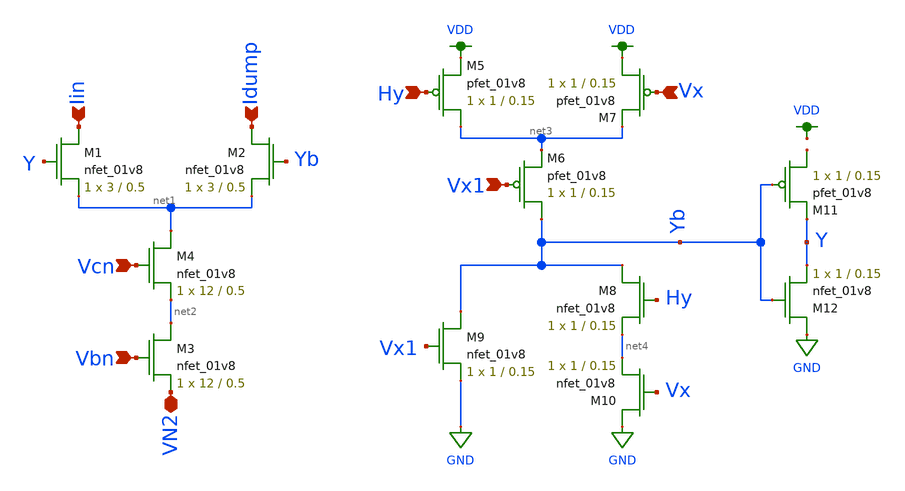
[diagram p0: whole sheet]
** sch_path: xschem/current_steering_unit_cell_with_decoder_for_lvs.sch
**.subckt current_steering_unit_cell_with_decoder_for_lvs Vcn Iin Idump Vbn Vx Vx1 Hy VN2
*.ipin Vcn
*.ipin Iin
*.ipin Idump
*.ipin Vbn
*.ipin Vx
*.ipin Vx1
*.ipin Hy
*.iopin VN2
XM1 Iin Y net1 GND sky130_fd_pr__nfet_01v8 L=0.5 W=3 nf=1 ad='int((nf+1)/2) * W/nf * 0.29' as='int((nf+2)/2) * W/nf * 0.29'
+ pd='2*int((nf+1)/2) * (W/nf + 0.29)' ps='2*int((nf+2)/2) * (W/nf + 0.29)' nrd='0.29 / W' nrs='0.29 / W'
+ sa=0 sb=0 sd=0 mult=1 m=1
XM2 Idump Yb net1 GND sky130_fd_pr__nfet_01v8 L=0.5 W=3 nf=1 ad='int((nf+1)/2) * W/nf * 0.29' as='int((nf+2)/2) * W/nf * 0.29'
+ pd='2*int((nf+1)/2) * (W/nf + 0.29)' ps='2*int((nf+2)/2) * (W/nf + 0.29)' nrd='0.29 / W' nrs='0.29 / W'
+ sa=0 sb=0 sd=0 mult=1 m=1
XM3 net2 Vbn VN2 GND sky130_fd_pr__nfet_01v8 L=0.5 W=12 nf=1 ad='int((nf+1)/2) * W/nf * 0.29' as='int((nf+2)/2) * W/nf * 0.29'
+ pd='2*int((nf+1)/2) * (W/nf + 0.29)' ps='2*int((nf+2)/2) * (W/nf + 0.29)' nrd='0.29 / W' nrs='0.29 / W'
+ sa=0 sb=0 sd=0 mult=1 m=1
XM4 net1 Vcn net2 GND sky130_fd_pr__nfet_01v8 L=0.5 W=12 nf=1 ad='int((nf+1)/2) * W/nf * 0.29' as='int((nf+2)/2) * W/nf * 0.29'
+ pd='2*int((nf+1)/2) * (W/nf + 0.29)' ps='2*int((nf+2)/2) * (W/nf + 0.29)' nrd='0.29 / W' nrs='0.29 / W'
+ sa=0 sb=0 sd=0 mult=1 m=1
XM5 net3 Hy VDD VDD sky130_fd_pr__pfet_01v8 L=0.15 W=1 nf=1 ad='int((nf+1)/2) * W/nf * 0.29' as='int((nf+2)/2) * W/nf * 0.29'
+ pd='2*int((nf+1)/2) * (W/nf + 0.29)' ps='2*int((nf+2)/2) * (W/nf + 0.29)' nrd='0.29 / W' nrs='0.29 / W'
+ sa=0 sb=0 sd=0 mult=1 m=1
XM6 Yb Vx1 net3 VDD sky130_fd_pr__pfet_01v8 L=0.15 W=1 nf=1 ad='int((nf+1)/2) * W/nf * 0.29' as='int((nf+2)/2) * W/nf * 0.29'
+ pd='2*int((nf+1)/2) * (W/nf + 0.29)' ps='2*int((nf+2)/2) * (W/nf + 0.29)' nrd='0.29 / W' nrs='0.29 / W'
+ sa=0 sb=0 sd=0 mult=1 m=1
XM7 VDD Vx net3 VDD sky130_fd_pr__pfet_01v8 L=0.15 W=1 nf=1 ad='int((nf+1)/2) * W/nf * 0.29' as='int((nf+2)/2) * W/nf * 0.29'
+ pd='2*int((nf+1)/2) * (W/nf + 0.29)' ps='2*int((nf+2)/2) * (W/nf + 0.29)' nrd='0.29 / W' nrs='0.29 / W'
+ sa=0 sb=0 sd=0 mult=1 m=1
XM8 Yb Hy net4 GND sky130_fd_pr__nfet_01v8 L=0.15 W=1 nf=1 ad='int((nf+1)/2) * W/nf * 0.29' as='int((nf+2)/2) * W/nf * 0.29'
+ pd='2*int((nf+1)/2) * (W/nf + 0.29)' ps='2*int((nf+2)/2) * (W/nf + 0.29)' nrd='0.29 / W' nrs='0.29 / W'
+ sa=0 sb=0 sd=0 mult=1 m=1
XM9 Yb Vx1 GND GND sky130_fd_pr__nfet_01v8 L=0.15 W=1 nf=1 ad='int((nf+1)/2) * W/nf * 0.29' as='int((nf+2)/2) * W/nf * 0.29'
+ pd='2*int((nf+1)/2) * (W/nf + 0.29)' ps='2*int((nf+2)/2) * (W/nf + 0.29)' nrd='0.29 / W' nrs='0.29 / W'
+ sa=0 sb=0 sd=0 mult=1 m=1
XM10 GND Vx net4 GND sky130_fd_pr__nfet_01v8 L=0.15 W=1 nf=1 ad='int((nf+1)/2) * W/nf * 0.29' as='int((nf+2)/2) * W/nf * 0.29'
+ pd='2*int((nf+1)/2) * (W/nf + 0.29)' ps='2*int((nf+2)/2) * (W/nf + 0.29)' nrd='0.29 / W' nrs='0.29 / W'
+ sa=0 sb=0 sd=0 mult=1 m=1
XM11 net5 Yb Y VDD sky130_fd_pr__pfet_01v8 L=0.15 W=1 nf=1 ad='int((nf+1)/2) * W/nf * 0.29' as='int((nf+2)/2) * W/nf * 0.29'
+ pd='2*int((nf+1)/2) * (W/nf + 0.29)' ps='2*int((nf+2)/2) * (W/nf + 0.29)' nrd='0.29 / W' nrs='0.29 / W'
+ sa=0 sb=0 sd=0 mult=1 m=1
XM12 GND Yb Y GND sky130_fd_pr__nfet_01v8 L=0.15 W=1 nf=1 ad='int((nf+1)/2) * W/nf * 0.29' as='int((nf+2)/2) * W/nf * 0.29'
+ pd='2*int((nf+1)/2) * (W/nf + 0.29)' ps='2*int((nf+2)/2) * (W/nf + 0.29)' nrd='0.29 / W' nrs='0.29 / W'
+ sa=0 sb=0 sd=0 mult=1 m=1
**.ends
.GLOBAL VDD
.GLOBAL GND
.end
